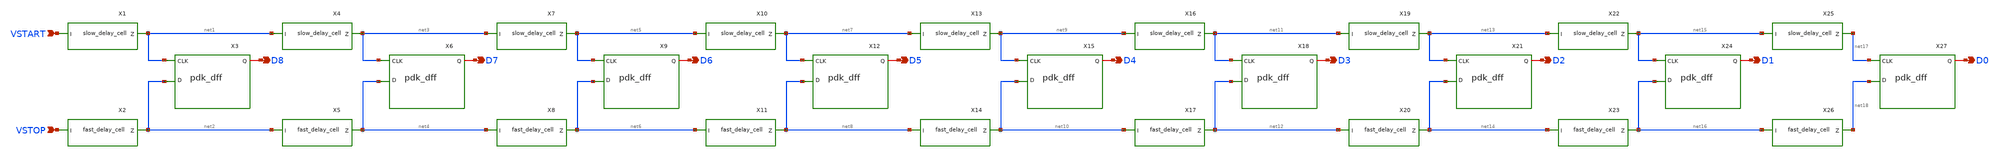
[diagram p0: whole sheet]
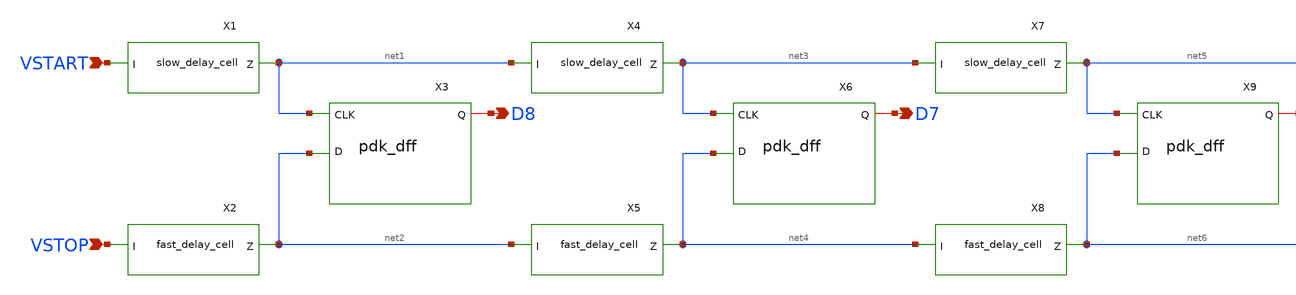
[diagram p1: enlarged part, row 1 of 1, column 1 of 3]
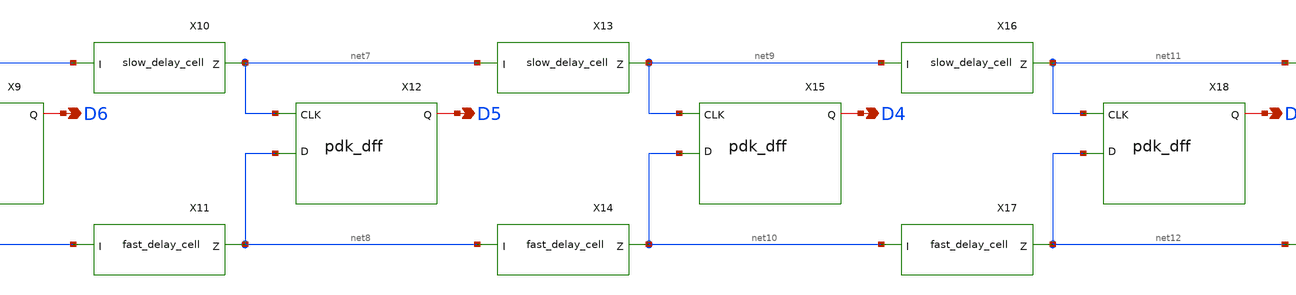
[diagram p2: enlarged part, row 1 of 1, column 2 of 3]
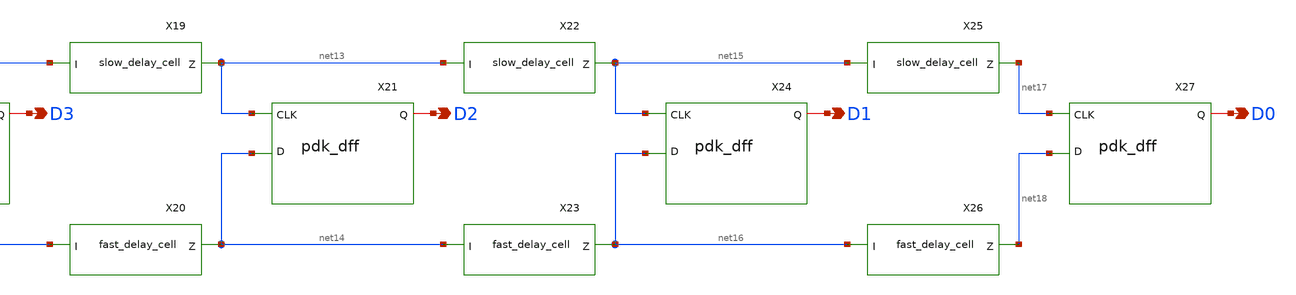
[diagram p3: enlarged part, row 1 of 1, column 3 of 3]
** sch_path: schem/fine_delay_line.sch
**.subckt fine_delay_line VSTART VSTOP D0 D1 D2 D3 D4 D5 D6 D7 D8
*.ipin VSTART
*.ipin VSTOP
*.opin D0
*.opin D1
*.opin D2
*.opin D3
*.opin D4
*.opin D5
*.opin D6
*.opin D7
*.opin D8
X1 VSTART net1 VDD VDD 0 0 gf180mcu_fd_sc_mcu7t5v0__dlya_4
X2 VSTOP net2 VDD VDD 0 0 gf180mcu_fd_sc_mcu7t5v0__dlya_1
X3 net2 net1 D8 VDD VDD 0 0 gf180mcu_fd_sc_mcu7t5v0__dffq_1
X4 net1 net3 VDD VDD 0 0 gf180mcu_fd_sc_mcu7t5v0__dlya_4
X5 net2 net4 VDD VDD 0 0 gf180mcu_fd_sc_mcu7t5v0__dlya_1
X6 net4 net3 D7 VDD VDD 0 0 gf180mcu_fd_sc_mcu7t5v0__dffq_1
X7 net3 net5 VDD VDD 0 0 gf180mcu_fd_sc_mcu7t5v0__dlya_4
X8 net4 net6 VDD VDD 0 0 gf180mcu_fd_sc_mcu7t5v0__dlya_1
X9 net6 net5 D6 VDD VDD 0 0 gf180mcu_fd_sc_mcu7t5v0__dffq_1
X10 net5 net7 VDD VDD 0 0 gf180mcu_fd_sc_mcu7t5v0__dlya_4
X11 net6 net8 VDD VDD 0 0 gf180mcu_fd_sc_mcu7t5v0__dlya_1
X12 net8 net7 D5 VDD VDD 0 0 gf180mcu_fd_sc_mcu7t5v0__dffq_1
X13 net7 net9 VDD VDD 0 0 gf180mcu_fd_sc_mcu7t5v0__dlya_4
X14 net8 net10 VDD VDD 0 0 gf180mcu_fd_sc_mcu7t5v0__dlya_1
X15 net10 net9 D4 VDD VDD 0 0 gf180mcu_fd_sc_mcu7t5v0__dffq_1
X16 net9 net11 VDD VDD 0 0 gf180mcu_fd_sc_mcu7t5v0__dlya_4
X17 net10 net12 VDD VDD 0 0 gf180mcu_fd_sc_mcu7t5v0__dlya_1
X18 net12 net11 D3 VDD VDD 0 0 gf180mcu_fd_sc_mcu7t5v0__dffq_1
X19 net11 net13 VDD VDD 0 0 gf180mcu_fd_sc_mcu7t5v0__dlya_4
X20 net12 net14 VDD VDD 0 0 gf180mcu_fd_sc_mcu7t5v0__dlya_1
X21 net14 net13 D2 VDD VDD 0 0 gf180mcu_fd_sc_mcu7t5v0__dffq_1
X22 net13 net15 VDD VDD 0 0 gf180mcu_fd_sc_mcu7t5v0__dlya_4
X23 net14 net16 VDD VDD 0 0 gf180mcu_fd_sc_mcu7t5v0__dlya_1
X24 net16 net15 D1 VDD VDD 0 0 gf180mcu_fd_sc_mcu7t5v0__dffq_1
X25 net15 net17 VDD VDD 0 0 gf180mcu_fd_sc_mcu7t5v0__dlya_4
X26 net16 net18 VDD VDD 0 0 gf180mcu_fd_sc_mcu7t5v0__dlya_1
X27 net18 net17 D0 VDD VDD 0 0 gf180mcu_fd_sc_mcu7t5v0__dffq_1
**.ends
.end
